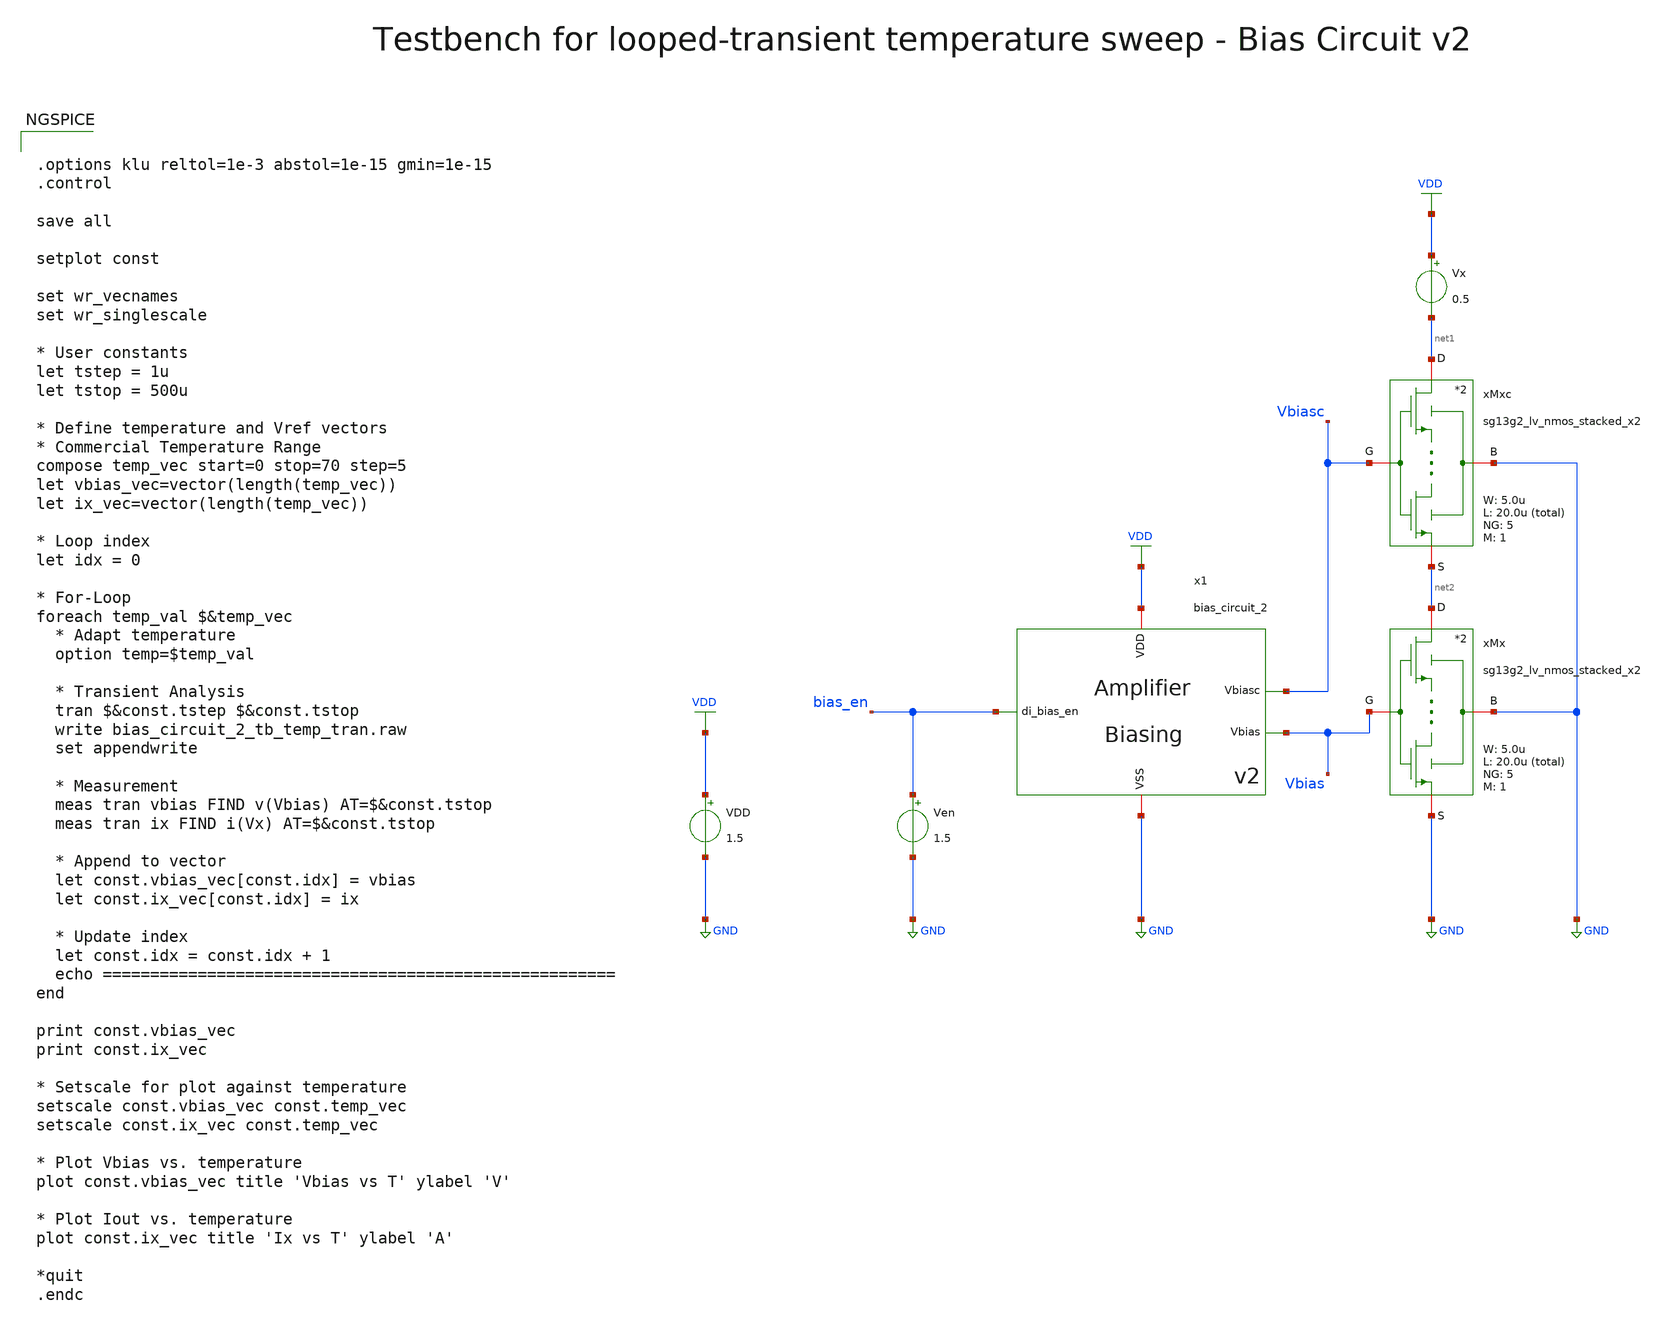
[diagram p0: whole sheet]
** sch_path: SG13G2_ATBS-ADC-main/xschem/bio_amplifier/amplifier_core/bias_circuit/bias_circuit_2/testbenches/bias_circuit_2_tb_temp_tran.sch
**.subckt bias_circuit_2_tb_temp_tran
Ven bias_en GND 1.5
VDD VDD GND 1.5
x1 bias_en Vbiasc VDD GND Vbias bias_circuit_2
Vx VDD net1 0.5
xMx net2 Vbias GND GND sg13g2_lv_nmos_stacked_x2 W_N=5.0u L_N=20.0u NG_N=5 M_N=1
xMxc net1 Vbiasc GND net2 sg13g2_lv_nmos_stacked_x2 W_N=5.0u L_N=20.0u NG_N=5 M_N=1
**** begin user architecture code

.lib cornerMOSlv.lib mos_tt
.lib cornerRES.lib res_typ



.options klu reltol=1e-3 abstol=1e-15 gmin=1e-15
.control

save all

setplot const

set wr_vecnames
set wr_singlescale

* User constants
let tstep = 1u
let tstop = 500u

* Define temperature and Vref vectors
* Commercial Temperature Range
compose temp_vec start=0 stop=70 step=5
let vbias_vec=vector(length(temp_vec))
let ix_vec=vector(length(temp_vec))

* Loop index
let idx = 0

* For-Loop
foreach temp_val $&temp_vec
  * Adapt temperature
  option temp=$temp_val

  * Transient Analysis
  tran $&const.tstep $&const.tstop
  write bias_circuit_2_tb_temp_tran.raw
  set appendwrite

  * Measurement
  meas tran vbias FIND v(Vbias) AT=$&const.tstop
  meas tran ix FIND i(Vx) AT=$&const.tstop

  * Append to vector
  let const.vbias_vec[const.idx] = vbias
  let const.ix_vec[const.idx] = ix

  * Update index
  let const.idx = const.idx + 1
  echo ======================================================
end

print const.vbias_vec
print const.ix_vec

* Setscale for plot against temperature
setscale const.vbias_vec const.temp_vec
setscale const.ix_vec const.temp_vec

* Plot Vbias vs. temperature
plot const.vbias_vec title 'Vbias vs T' ylabel 'V'

* Plot Iout vs. temperature
plot const.ix_vec title 'Ix vs T' ylabel 'A'

*quit
.endc

**** end user architecture code
**.ends

* expanding   symbol:  bio_amplifier/amplifier_core/bias_circuit/bias_circuit_2/bias_circuit_2.sym #
*+ of pins=5
** sym_path: SG13G2_ATBS-ADC-main/xschem/bio_amplifier/amplifier_core/bias_circuit/bias_circuit_2/bias_circuit_2.sym
** sch_path: SG13G2_ATBS-ADC-main/xschem/bio_amplifier/amplifier_core/bias_circuit/bias_circuit_2/bias_circuit_2.sch
.subckt bias_circuit_2 di_bias_en Vbiasc VDD VSS Vbias
*.iopin VDD
*.iopin VSS
*.opin Vbias
*.ipin di_bias_en
*.opin Vbiasc
R1 net3 VSS 3.72Meg m=1
XMDEC1 net1 Vbias net1 net1 sg13_lv_nmos w=100.0u l=40.0u ng=100 m=1 mm_ok=1
VIref net4 net8 0
.save i(viref)
VIout net9 Vbiasc 0
.save i(viout)
x1 VDD di_bias_en bias_en_n VSS inverter_lv W_P=1.0u L_P=0.13u W_N=1.0u L_N=0.13u
xMSU2 Vsu net6 VSS VSS sg13g2_lv_nmos_stacked_x4 W_N=1.0u L_N=40.0u NG_N=1 M_N=1
xMSU1 net5 Vsu VSS net6 sg13g2_lv_nmos_stacked_x4 W_N=1.0u L_N=40.0u NG_N=1 M_N=1
Vmeas1 net4 net5 0
.save i(vmeas1)
Vmeas2 Vbias net6 0
.save i(vmeas2)
XMPD1 Vgs_m34 di_bias_en net2 net2 sg13_lv_pmos w=1.0u l=0.13u ng=1 m=1 mm_ok=1
XMPD2 net4 bias_en_n Vgs_m34 net2 sg13_lv_pmos w=1.0u l=0.13u ng=1 m=1 mm_ok=1
XMPD3 Vbias bias_en_n VSS VSS sg13_lv_nmos w=1.0u l=0.13u ng=1 m=1 mm_ok=1
VIref5 net1 VSS 0
.save i(viref5)
VIdd VDD net2 0
.save i(vidd)
CSU1 net10 Vsu 35f m=1
xM1 net7 Vbias VSS net3 sg13g2_lv_nmos_stacked_x2 W_N=20.0u L_N=20.0u NG_N=20 M_N=1
xM1c net8 Vbiasc VSS net7 sg13g2_lv_nmos_stacked_x2 W_N=5.0u L_N=20.0u NG_N=5 M_N=1
xM2 Vbias Vbias VSS VSS sg13g2_lv_nmos_stacked_x2 W_N=5.0u L_N=20.0u NG_N=5 M_N=1
xM2c Vbiasc Vbiasc VSS Vbias sg13g2_lv_nmos_stacked_x2 W_N=5.0u L_N=20.0u NG_N=5 M_N=1
XMDEC2 net2 Vgs_m34 net2 net2 sg13_lv_pmos w=25.0u l=40.0u ng=25 m=1 mm_ok=1
xM3 net4 Vgs_m34 net2 net2 sg13g2_lv_pmos_stacked_x4 W_P=20.0u L_P=40.0u NG_P=20 M_P=1
xM4 net9 Vgs_m34 net2 net2 sg13g2_lv_pmos_stacked_x4 W_P=20.0u L_P=40.0u NG_P=20 M_P=1
XMPD6 Vsu di_bias_en net10 net10 sg13_lv_pmos w=1.0u l=0.13u ng=1 m=1 mm_ok=1
XMPD4 Vbiasc bias_en_n VSS VSS sg13_lv_nmos w=1.0u l=0.13u ng=1 m=1 mm_ok=1
XMPD7 Vsu bias_en_n VSS VSS sg13_lv_nmos w=1.0u l=0.13u ng=1 m=1 mm_ok=1
XMPD5 net10 bias_en_n net2 net2 sg13_lv_pmos w=1.0u l=0.13u ng=1 m=1 mm_ok=1
.ends


* expanding   symbol:  stacked_transistors/sg13g2_lv_nmos_stacked/sg13g2_lv_nmos_stacked_x2.sym # of
*+ pins=4
** sym_path: SG13G2_ATBS-ADC-main/xschem/stacked_transistors/sg13g2_lv_nmos_stacked/sg13g2_lv_nmos_stacked_x2.sym
** sch_path: SG13G2_ATBS-ADC-main/xschem/stacked_transistors/sg13g2_lv_nmos_stacked/sg13g2_lv_nmos_stacked_x2.sch
.subckt sg13g2_lv_nmos_stacked_x2 D G B S  W_N=1.0u L_N=0.45u NG_N=1 M_N=1
*.iopin D
*.iopin S
*.iopin G
*.iopin B
XM1 net1 G S B sg13_lv_nmos w=W_N l=L_N/2 ng=NG_N m=M_N mm_ok=1
XM2 D G net1 B sg13_lv_nmos w=W_N l=L_N/2 ng=NG_N m=M_N mm_ok=1
.ends


* expanding   symbol:  inverter/inverter_lv.sym # of pins=4
** sym_path: SG13G2_ATBS-ADC-main/xschem/inverter/inverter_lv.sym
** sch_path: SG13G2_ATBS-ADC-main/xschem/inverter/inverter_lv.sch
.subckt inverter_lv VDD vin vout VSS  W_P=3.0u L_P=0.13u W_N=1.0u L_N=0.13u
*.ipin vin
*.iopin VDD
*.iopin VSS
*.opin vout
XM1 vout vin VDD VDD sg13_lv_pmos w=W_P l=L_P ng=1 m=1 mm_ok=1
XM2 vout vin VSS VSS sg13_lv_nmos w=W_N l=L_N ng=1 m=1 mm_ok=1
.ends


* expanding   symbol:  stacked_transistors/sg13g2_lv_nmos_stacked/sg13g2_lv_nmos_stacked_x4.sym # of
*+ pins=4
** sym_path: SG13G2_ATBS-ADC-main/xschem/stacked_transistors/sg13g2_lv_nmos_stacked/sg13g2_lv_nmos_stacked_x4.sym
** sch_path: SG13G2_ATBS-ADC-main/xschem/stacked_transistors/sg13g2_lv_nmos_stacked/sg13g2_lv_nmos_stacked_x4.sch
.subckt sg13g2_lv_nmos_stacked_x4 D G B S  W_N=1.0u L_N=0.45u NG_N=1 M_N=1
*.iopin D
*.iopin S
*.iopin G
*.iopin B
XM1 net1 G S B sg13_lv_nmos w=W_N l=L_N/4 ng=NG_N m=M_N mm_ok=1
XM2 net3 G net1 B sg13_lv_nmos w=W_N l=L_N/4 ng=NG_N m=M_N mm_ok=1
XM3 net2 G net3 B sg13_lv_nmos w=W_N l=L_N/4 ng=NG_N m=M_N mm_ok=1
XM4 D G net2 B sg13_lv_nmos w=W_N l=L_N/4 ng=NG_N m=M_N mm_ok=1
.ends


* expanding   symbol:  stacked_transistors/sg13g2_lv_pmos_stacked/sg13g2_lv_pmos_stacked_x4.sym # of
*+ pins=4
** sym_path: SG13G2_ATBS-ADC-main/xschem/stacked_transistors/sg13g2_lv_pmos_stacked/sg13g2_lv_pmos_stacked_x4.sym
** sch_path: SG13G2_ATBS-ADC-main/xschem/stacked_transistors/sg13g2_lv_pmos_stacked/sg13g2_lv_pmos_stacked_x4.sch
.subckt sg13g2_lv_pmos_stacked_x4 D G B S  W_P=1.0u L_P=0.45u NG_P=1 M_P=1
*.iopin D
*.iopin S
*.iopin G
*.iopin B
XM1 net1 G S B sg13_lv_pmos w=W_P l=L_P/4 ng=NG_P m=M_P mm_ok=1
XM2 net3 G net1 B sg13_lv_pmos w=W_P l=L_P/4 ng=NG_P m=M_P mm_ok=1
XM3 net2 G net3 B sg13_lv_pmos w=W_P l=L_P/4 ng=NG_P m=M_P mm_ok=1
XM4 D G net2 B sg13_lv_pmos w=W_P l=L_P/4 ng=NG_P m=M_P mm_ok=1
.ends

.GLOBAL GND
.GLOBAL VDD
.end
